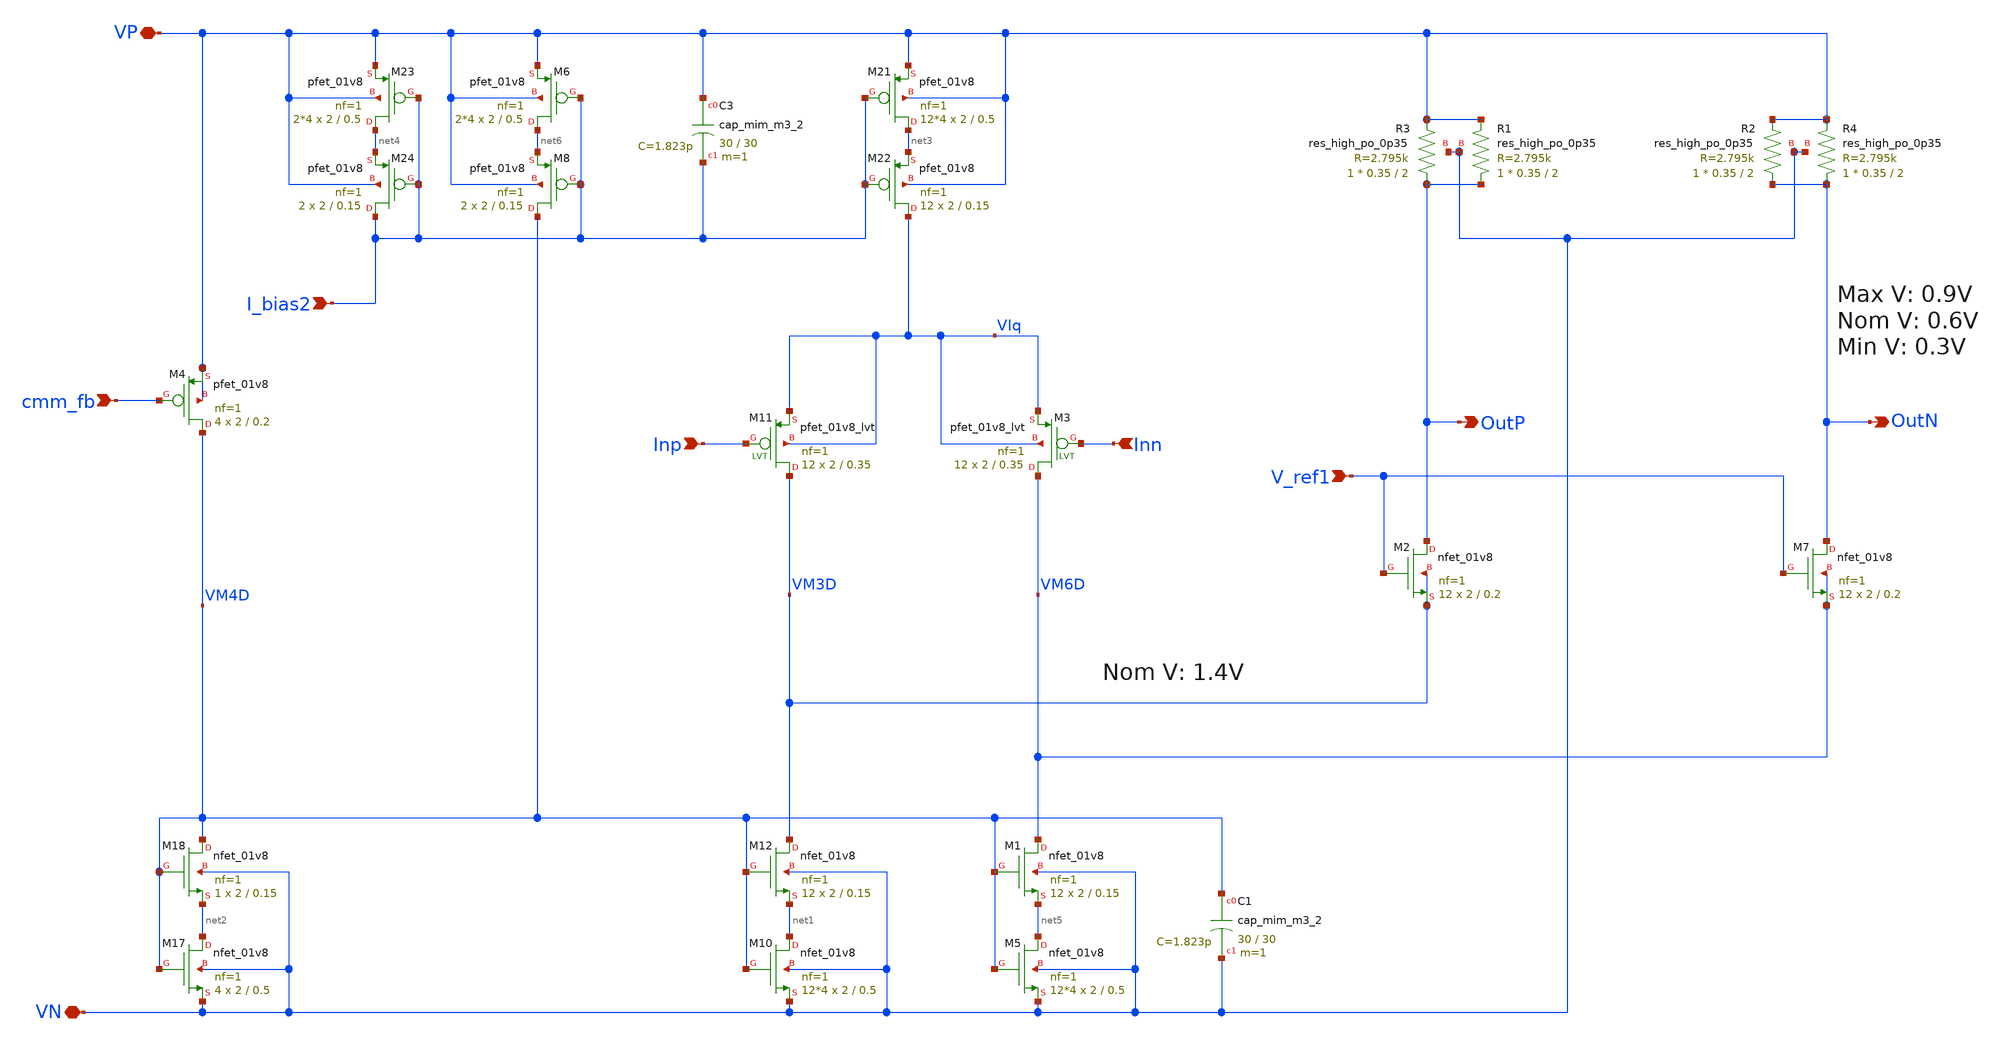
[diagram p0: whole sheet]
** sch_path: xschem/comp/comp_casc_p.sch
**.subckt comp_casc_p Inp cmm_fb Inn VP VN OutN OutP V_ref1 I_bias2
*.ipin Inp
*.ipin cmm_fb
*.ipin Inn
*.iopin VP
*.iopin VN
*.opin OutN
*.opin OutP
*.ipin V_ref1
*.ipin I_bias2
XM10 net1 VM4D VN VN sky130_fd_pr__nfet_01v8 L=0.5 W=2 nf=1 ad='int((nf+1)/2) * W/nf * 0.29' as='int((nf+2)/2) * W/nf * 0.29'
+ pd='2*int((nf+1)/2) * (W/nf + 0.29)' ps='2*int((nf+2)/2) * (W/nf + 0.29)' nrd='0.29 / W' nrs='0.29 / W'
+ sa=0 sb=0 sd=0 mult=12*4 m=12*4
XM12 VM3D VM4D net1 VN sky130_fd_pr__nfet_01v8 L=0.15 W=2 nf=1 ad='int((nf+1)/2) * W/nf * 0.29' as='int((nf+2)/2) * W/nf * 0.29'
+ pd='2*int((nf+1)/2) * (W/nf + 0.29)' ps='2*int((nf+2)/2) * (W/nf + 0.29)' nrd='0.29 / W' nrs='0.29 / W'
+ sa=0 sb=0 sd=0 mult=12 m=12
XM17 net2 VM4D VN VN sky130_fd_pr__nfet_01v8 L=0.5 W=2 nf=1 ad='int((nf+1)/2) * W/nf * 0.29' as='int((nf+2)/2) * W/nf * 0.29'
+ pd='2*int((nf+1)/2) * (W/nf + 0.29)' ps='2*int((nf+2)/2) * (W/nf + 0.29)' nrd='0.29 / W' nrs='0.29 / W'
+ sa=0 sb=0 sd=0 mult=4 m=4
XM18 VM4D VM4D net2 VN sky130_fd_pr__nfet_01v8 L=0.15 W=2 nf=1 ad='int((nf+1)/2) * W/nf * 0.29' as='int((nf+2)/2) * W/nf * 0.29'
+ pd='2*int((nf+1)/2) * (W/nf + 0.29)' ps='2*int((nf+2)/2) * (W/nf + 0.29)' nrd='0.29 / W' nrs='0.29 / W'
+ sa=0 sb=0 sd=0 mult=1 m=1
XC1 VM4D VN sky130_fd_pr__cap_mim_m3_2 W=30 L=30 MF=1 m=1
XR3 OutP VP VN sky130_fd_pr__res_high_po_0p35 L=2 mult=1 m=1
XR4 OutN VP VN sky130_fd_pr__res_high_po_0p35 L=2 mult=1 m=1
XM21 net3 I_bias2 VP VP sky130_fd_pr__pfet_01v8 L=0.5 W=2 nf=1 ad='int((nf+1)/2) * W/nf * 0.29' as='int((nf+2)/2) * W/nf * 0.29'
+ pd='2*int((nf+1)/2) * (W/nf + 0.29)' ps='2*int((nf+2)/2) * (W/nf + 0.29)' nrd='0.29 / W' nrs='0.29 / W'
+ sa=0 sb=0 sd=0 mult=12*4 m=12*4
XM22 VIq I_bias2 net3 VP sky130_fd_pr__pfet_01v8 L=0.15 W=2 nf=1 ad='int((nf+1)/2) * W/nf * 0.29' as='int((nf+2)/2) * W/nf * 0.29'
+ pd='2*int((nf+1)/2) * (W/nf + 0.29)' ps='2*int((nf+2)/2) * (W/nf + 0.29)' nrd='0.29 / W' nrs='0.29 / W'
+ sa=0 sb=0 sd=0 mult=12 m=12
XM23 net4 I_bias2 VP VP sky130_fd_pr__pfet_01v8 L=0.5 W=2 nf=1 ad='int((nf+1)/2) * W/nf * 0.29' as='int((nf+2)/2) * W/nf * 0.29'
+ pd='2*int((nf+1)/2) * (W/nf + 0.29)' ps='2*int((nf+2)/2) * (W/nf + 0.29)' nrd='0.29 / W' nrs='0.29 / W'
+ sa=0 sb=0 sd=0 mult=2*4 m=2*4
XM24 I_bias2 I_bias2 net4 VP sky130_fd_pr__pfet_01v8 L=0.15 W=2 nf=1 ad='int((nf+1)/2) * W/nf * 0.29'
+ as='int((nf+2)/2) * W/nf * 0.29' pd='2*int((nf+1)/2) * (W/nf + 0.29)' ps='2*int((nf+2)/2) * (W/nf + 0.29)'
+ nrd='0.29 / W' nrs='0.29 / W' sa=0 sb=0 sd=0 mult=2 m=2
XC3 VP I_bias2 sky130_fd_pr__cap_mim_m3_2 W=30 L=30 MF=1 m=1
XM2 OutP V_ref1 VM3D VM3D sky130_fd_pr__nfet_01v8 L=0.2 W=2 nf=1 ad='int((nf+1)/2) * W/nf * 0.29' as='int((nf+2)/2) * W/nf * 0.29'
+ pd='2*int((nf+1)/2) * (W/nf + 0.29)' ps='2*int((nf+2)/2) * (W/nf + 0.29)' nrd='0.29 / W' nrs='0.29 / W'
+ sa=0 sb=0 sd=0 mult=12 m=12
XM4 VM4D cmm_fb VP VP sky130_fd_pr__pfet_01v8 L=0.2 W=2 nf=1 ad='int((nf+1)/2) * W/nf * 0.29' as='int((nf+2)/2) * W/nf * 0.29'
+ pd='2*int((nf+1)/2) * (W/nf + 0.29)' ps='2*int((nf+2)/2) * (W/nf + 0.29)' nrd='0.29 / W' nrs='0.29 / W'
+ sa=0 sb=0 sd=0 mult=4 m=4
XM7 OutN V_ref1 VM6D VM6D sky130_fd_pr__nfet_01v8 L=0.2 W=2 nf=1 ad='int((nf+1)/2) * W/nf * 0.29' as='int((nf+2)/2) * W/nf * 0.29'
+ pd='2*int((nf+1)/2) * (W/nf + 0.29)' ps='2*int((nf+2)/2) * (W/nf + 0.29)' nrd='0.29 / W' nrs='0.29 / W'
+ sa=0 sb=0 sd=0 mult=12 m=12
XM11 VM3D Inp VIq VIq sky130_fd_pr__pfet_01v8_lvt L=0.35 W=2 nf=1 ad='int((nf+1)/2) * W/nf * 0.29' as='int((nf+2)/2) * W/nf * 0.29'
+ pd='2*int((nf+1)/2) * (W/nf + 0.29)' ps='2*int((nf+2)/2) * (W/nf + 0.29)' nrd='0.29 / W' nrs='0.29 / W'
+ sa=0 sb=0 sd=0 mult=12 m=12
XM3 VM6D Inn VIq VIq sky130_fd_pr__pfet_01v8_lvt L=0.35 W=2 nf=1 ad='int((nf+1)/2) * W/nf * 0.29' as='int((nf+2)/2) * W/nf * 0.29'
+ pd='2*int((nf+1)/2) * (W/nf + 0.29)' ps='2*int((nf+2)/2) * (W/nf + 0.29)' nrd='0.29 / W' nrs='0.29 / W'
+ sa=0 sb=0 sd=0 mult=12 m=12
XM1 VM6D VM4D net5 VN sky130_fd_pr__nfet_01v8 L=0.15 W=2 nf=1 ad='int((nf+1)/2) * W/nf * 0.29' as='int((nf+2)/2) * W/nf * 0.29'
+ pd='2*int((nf+1)/2) * (W/nf + 0.29)' ps='2*int((nf+2)/2) * (W/nf + 0.29)' nrd='0.29 / W' nrs='0.29 / W'
+ sa=0 sb=0 sd=0 mult=12 m=12
XM5 net5 VM4D VN VN sky130_fd_pr__nfet_01v8 L=0.5 W=2 nf=1 ad='int((nf+1)/2) * W/nf * 0.29' as='int((nf+2)/2) * W/nf * 0.29'
+ pd='2*int((nf+1)/2) * (W/nf + 0.29)' ps='2*int((nf+2)/2) * (W/nf + 0.29)' nrd='0.29 / W' nrs='0.29 / W'
+ sa=0 sb=0 sd=0 mult=12*4 m=12*4
XR1 OutP VP VN sky130_fd_pr__res_high_po_0p35 L=2 mult=1 m=1
XR2 OutN VP VN sky130_fd_pr__res_high_po_0p35 L=2 mult=1 m=1
XM6 net6 I_bias2 VP VP sky130_fd_pr__pfet_01v8 L=0.5 W=2 nf=1 ad='int((nf+1)/2) * W/nf * 0.29' as='int((nf+2)/2) * W/nf * 0.29'
+ pd='2*int((nf+1)/2) * (W/nf + 0.29)' ps='2*int((nf+2)/2) * (W/nf + 0.29)' nrd='0.29 / W' nrs='0.29 / W'
+ sa=0 sb=0 sd=0 mult=2*4 m=2*4
XM8 VM4D I_bias2 net6 VP sky130_fd_pr__pfet_01v8 L=0.15 W=2 nf=1 ad='int((nf+1)/2) * W/nf * 0.29' as='int((nf+2)/2) * W/nf * 0.29'
+ pd='2*int((nf+1)/2) * (W/nf + 0.29)' ps='2*int((nf+2)/2) * (W/nf + 0.29)' nrd='0.29 / W' nrs='0.29 / W'
+ sa=0 sb=0 sd=0 mult=2 m=2
**** begin user architecture code

*.lib $::SKYWATER_MODELS/sky130.lib.spice tt
.lib $::SKYWATER_MODELS/sky130.lib.spice.tt.red tt



*.options savecurrents
.option warn=1
.control
set wr_vecnames
set wr_singlescale
* Power consumption
op
* save all
* #OP#
print @m.xm1.msky130_fd_pr__nfet_01v8_lvt[gds]
print vdd#branch
print v(vm2d)
print v(vm3d)
print v(UD_M5)
wrdata 'result_op.csv' vdd#branch
ac dec 10 1 10G
meas ac dc_gain_vm2d FIND vdb(vm2d) AT=1
let bw_amp_vm2d=dc_gain_vm2d-3
meas ac dc_gain_vm3d FIND vdb(vm3d) AT=1
let bw_amp_vm3d=dc_gain_vm3d-3
meas ac bw_vm2d when vdb(vm2d)=bw_amp_vm2d
meas ac bw_vm3d when vdb(vm3d)=bw_amp_vm3d
*MEAS AC phasem FIND vp(vm2d) WHEN vdb(vm2d)=0
* wrdata 'result_ac.csv' dc_gain bw
* plot vdb(vm2D) log
*
*print WM3D
run
reset
save @m.xm1.msky130_fd_pr__nfet_01v8_lvt[gds]
save @m.xm1.msky130_fd_pr__nfet_01v8_lvt[gm]
save @m.xm1.msky130_fd_pr__nfet_01v8_lvt[cgs]
save @m.xm1.msky130_fd_pr__nfet_01v8_lvt[cdg]
save @m.xm2.msky130_fd_pr__nfet_01v8_lvt[gm]
save @m.xm2.msky130_fd_pr__nfet_01v8_lvt[gds]
save @m.xm2.msky130_fd_pr__nfet_01v8_lvt[cgs]
save @m.xm2.msky130_fd_pr__nfet_01v8_lvt[cdg]
save @m.xm3.msky130_fd_pr__nfet_01v8_lvt[gm]
save @m.xm3.msky130_fd_pr__nfet_01v8_lvt[gds]
save @m.xm3.msky130_fd_pr__nfet_01v8_lvt[cgs]
save @m.xm3.msky130_fd_pr__nfet_01v8_lvt[cdg]
save @m.xm4.msky130_fd_pr__nfet_01v8_lvt[gm]
save @m.xm4.msky130_fd_pr__nfet_01v8_lvt[gds]
save @m.xm4.msky130_fd_pr__nfet_01v8_lvt[cgs]
save @m.xm4.msky130_fd_pr__nfet_01v8_lvt[cdg]
save @m.xm5.msky130_fd_pr__pfet_01v8_lvt[gm]
save @m.xm5.msky130_fd_pr__pfet_01v8_lvt[gds]
save @m.xm5.msky130_fd_pr__pfet_01v8_lvt[cgs]
save @m.xm5.msky130_fd_pr__pfet_01v8_lvt[cdg]
save @m.xm6.msky130_fd_pr__pfet_01v8_lvt[gm]
save @m.xm6.msky130_fd_pr__pfet_01v8_lvt[gds]
save @m.xm6.msky130_fd_pr__pfet_01v8_lvt[cgs]
save @m.xm6.msky130_fd_pr__pfet_01v8_lvt[cdg]
save @m.xm7.msky130_fd_pr__nfet_01v8_lvt[gm]
save @m.xm7.msky130_fd_pr__nfet_01v8_lvt[gds]
save @m.xm7.msky130_fd_pr__nfet_01v8_lvt[cgs]
save @m.xm7.msky130_fd_pr__nfet_01v8_lvt[cdg]
save @m.xm8.msky130_fd_pr__nfet_01v8_lvt[gm]
save @m.xm8.msky130_fd_pr__nfet_01v8_lvt[gds]
save @m.xm8.msky130_fd_pr__nfet_01v8_lvt[cgs]
save @m.xm8.msky130_fd_pr__nfet_01v8_lvt[cdg]
save @m.xm9.msky130_fd_pr__nfet_01v8_lvt[gm]
save @m.xm9.msky130_fd_pr__nfet_01v8_lvt[gds]
save @m.xm9.msky130_fd_pr__nfet_01v8_lvt[cgs]
save @m.xm9.msky130_fd_pr__nfet_01v8_lvt[cdg]
save v(Voutp)
save v(Voutn)
save v(VIa)
save v(VIq)

save v(Vinn)
save v(Vinp)
save v(VM8G)

op
write comp.raw
run
*reset
*noise v(vm1d) I1 dec 100 1 10G
*print all
*setplot noise2
*write noise2.raw
*run
reset
ac dec 10 1 1T
plot vdb(Voutp) vdb(Voutn)
plot phase(Voutp)/pi*180 phase(Voutn)/pi*180
run
reset
tran 1ps 10ns
plot v(Vinp) v(Voutn) v(Voutp)
run
.endc


**** end user architecture code
**.ends
.end
